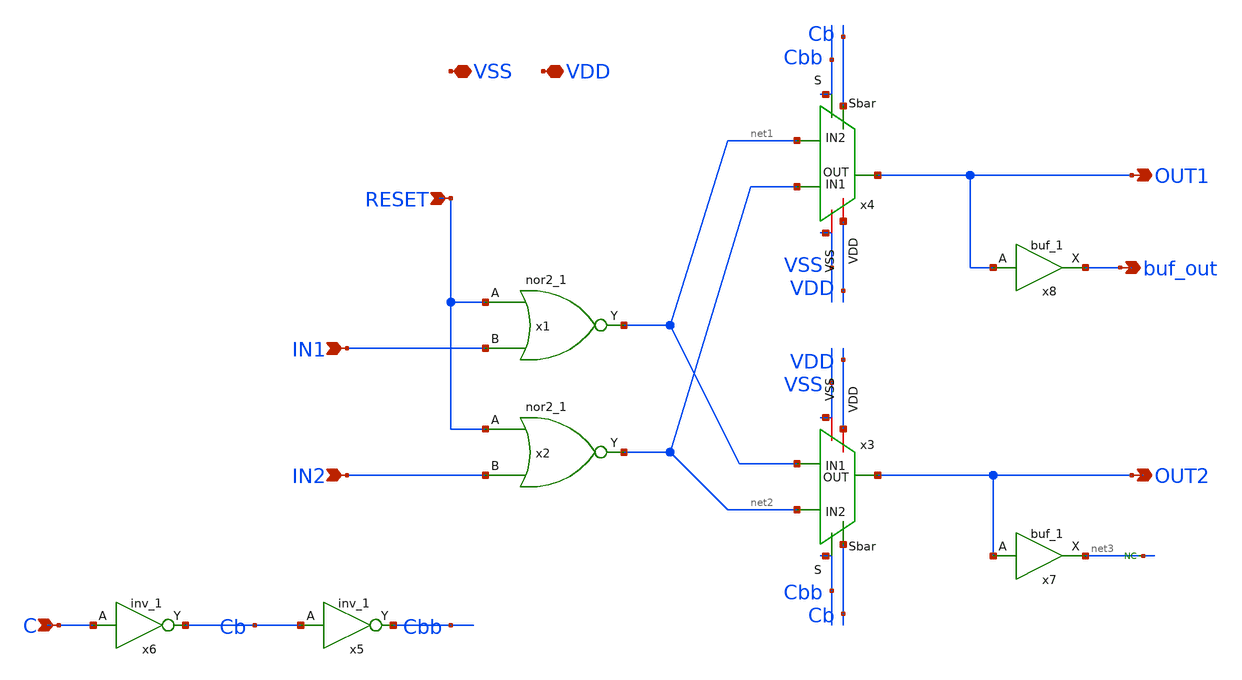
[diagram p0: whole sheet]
** sch_path: design/singlestage_nbr.sch
**.subckt singlestage_nbr IN1 C RESET VSS VDD OUT2 buf_out OUT1 IN2
*.ipin IN1
*.ipin C
*.ipin RESET
*.iopin VSS
*.iopin VDD
*.opin OUT2
*.opin buf_out
*.opin OUT1
*.ipin IN2
x1 RESET IN1 VSS VSS VDD VDD net1 sky130_fd_sc_hd__nor2_1
x2 RESET IN2 VSS VSS VDD VDD net2 sky130_fd_sc_hd__nor2_1
x5 Cb VSS VSS VDD VDD Cbb sky130_fd_sc_hd__inv_1
x6 C VSS VSS VDD VDD Cb sky130_fd_sc_hd__inv_1
x7 OUT2 VSS VSS VDD VDD net3 sky130_fd_sc_hd__buf_1
x3 Cbb VSS net1 VDD OUT2 Cb net2 mux2-1
x4 Cbb VSS net2 VDD OUT1 Cb net1 mux2-1
x8 OUT1 VSS VSS VDD VDD buf_out sky130_fd_sc_hd__buf_1
* noconn #net3
**.ends

* expanding   symbol:  mux2-1.sym # of pins=7
** sym_path: design/mux2-1.sym
** sch_path: design/mux2-1.sch
.subckt mux2-1 S VSS IN1 VDD OUT Sbar IN2
*.ipin IN1
*.ipin IN2
*.ipin Sbar
*.ipin S
*.opin OUT
*.iopin VSS
*.iopin VDD
XM2 IN1 S OUT VSS sky130_fd_pr__nfet_01v8 L=0.15 W=0.65 nf=1 ad='int((nf+1)/2) * W/nf * 0.29' as='int((nf+2)/2) * W/nf * 0.29'
+ pd='2*int((nf+1)/2) * (W/nf + 0.29)' ps='2*int((nf+2)/2) * (W/nf + 0.29)' nrd='0.29 / W' nrs='0.29 / W'
+ sa=0 sb=0 sd=0 mult=1 m=1
XM1 IN2 Sbar OUT VSS sky130_fd_pr__nfet_01v8 L=0.15 W=0.65 nf=1 ad='int((nf+1)/2) * W/nf * 0.29' as='int((nf+2)/2) * W/nf * 0.29'
+ pd='2*int((nf+1)/2) * (W/nf + 0.29)' ps='2*int((nf+2)/2) * (W/nf + 0.29)' nrd='0.29 / W' nrs='0.29 / W'
+ sa=0 sb=0 sd=0 mult=1 m=1
XM4 IN1 Sbar OUT VDD sky130_fd_pr__pfet_01v8_hvt L=0.15 W=1 nf=1 ad='int((nf+1)/2) * W/nf * 0.29' as='int((nf+2)/2) * W/nf * 0.29'
+ pd='2*int((nf+1)/2) * (W/nf + 0.29)' ps='2*int((nf+2)/2) * (W/nf + 0.29)' nrd='0.29 / W' nrs='0.29 / W'
+ sa=0 sb=0 sd=0 mult=1 m=1
XM5 IN2 S OUT VDD sky130_fd_pr__pfet_01v8_hvt L=0.15 W=1 nf=1 ad='int((nf+1)/2) * W/nf * 0.29' as='int((nf+2)/2) * W/nf * 0.29'
+ pd='2*int((nf+1)/2) * (W/nf + 0.29)' ps='2*int((nf+2)/2) * (W/nf + 0.29)' nrd='0.29 / W' nrs='0.29 / W'
+ sa=0 sb=0 sd=0 mult=1 m=1
.ends

.end
